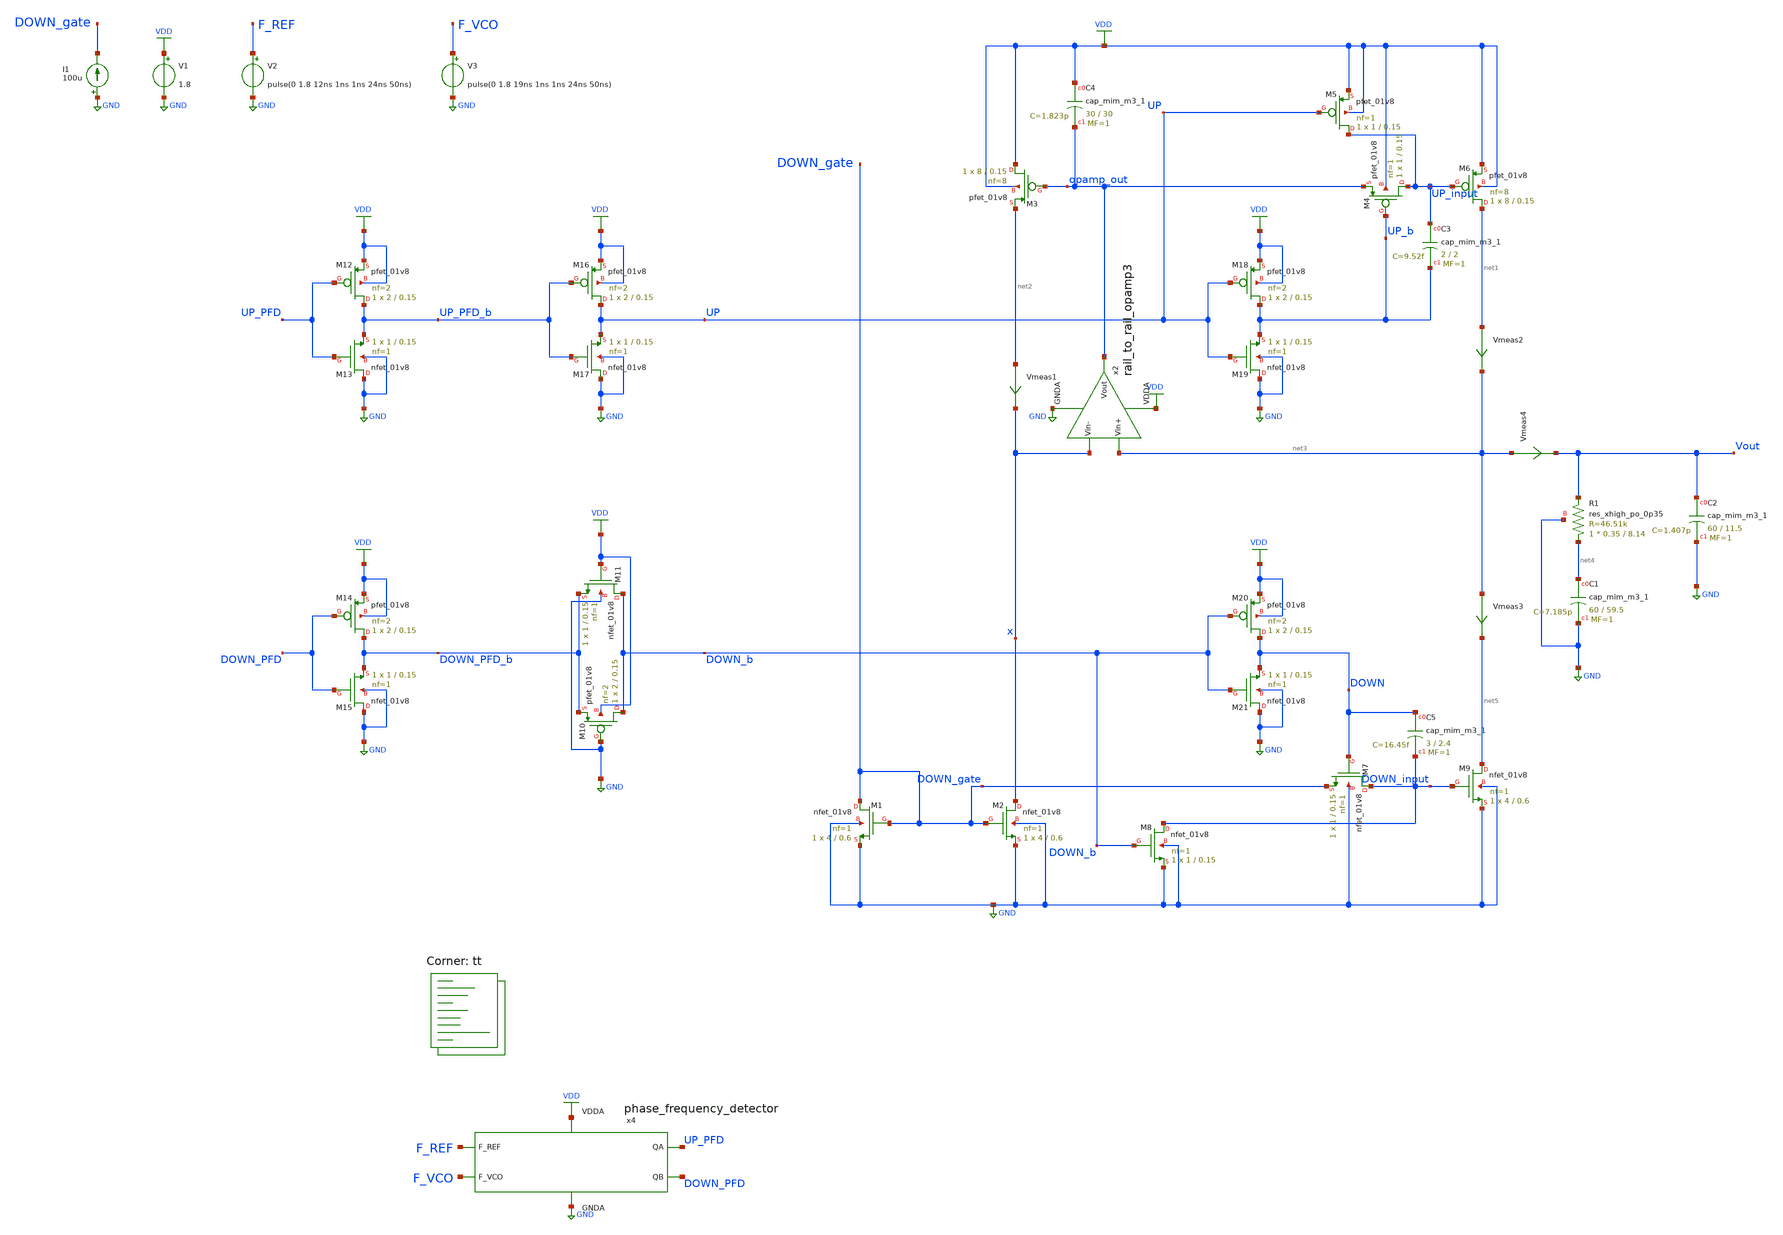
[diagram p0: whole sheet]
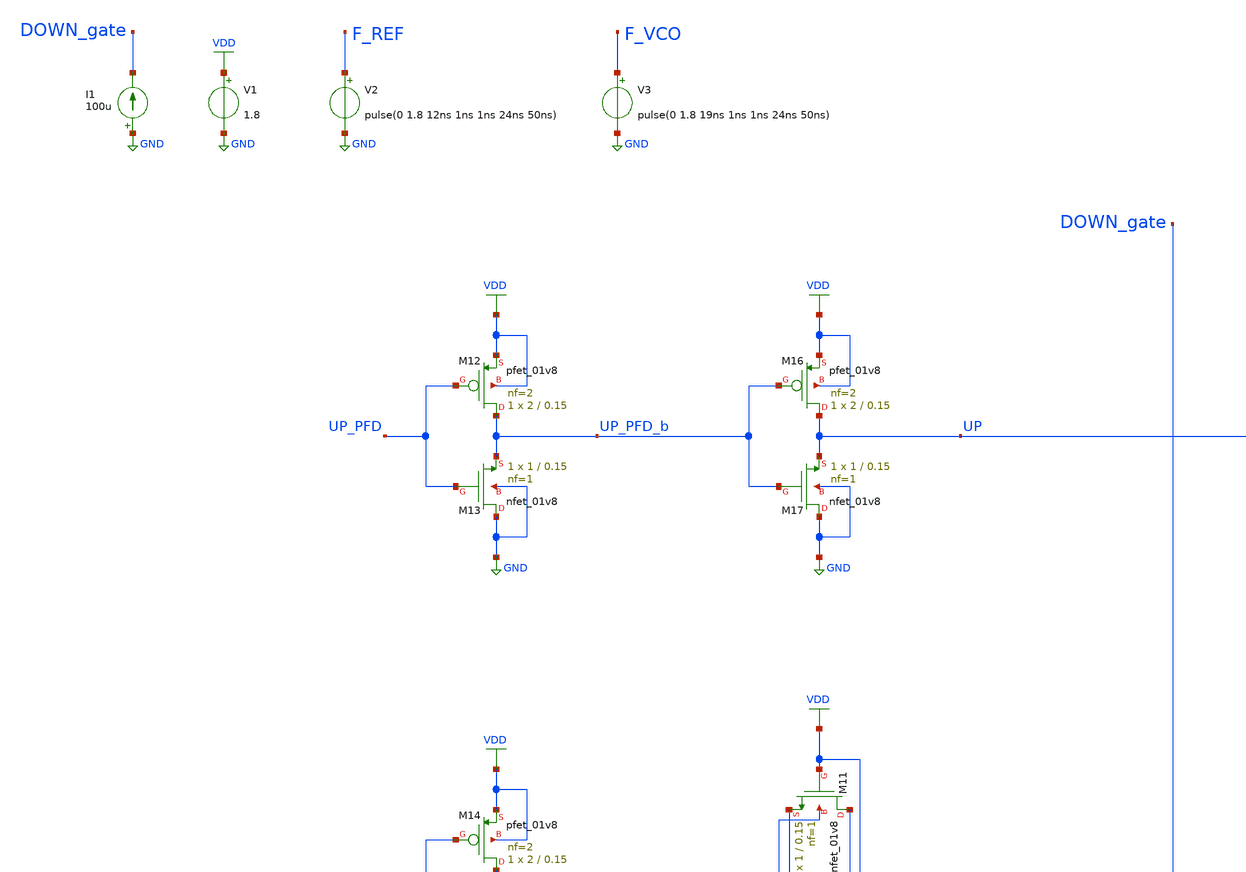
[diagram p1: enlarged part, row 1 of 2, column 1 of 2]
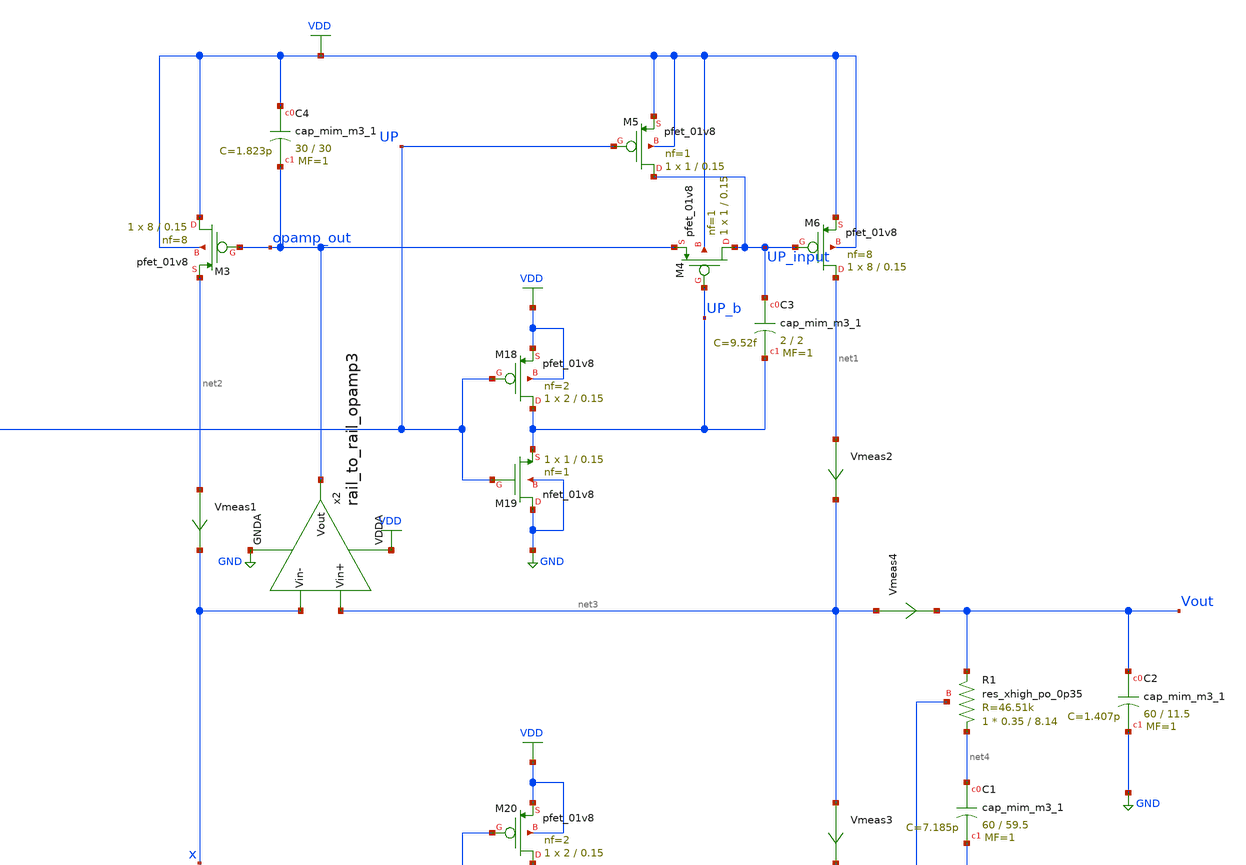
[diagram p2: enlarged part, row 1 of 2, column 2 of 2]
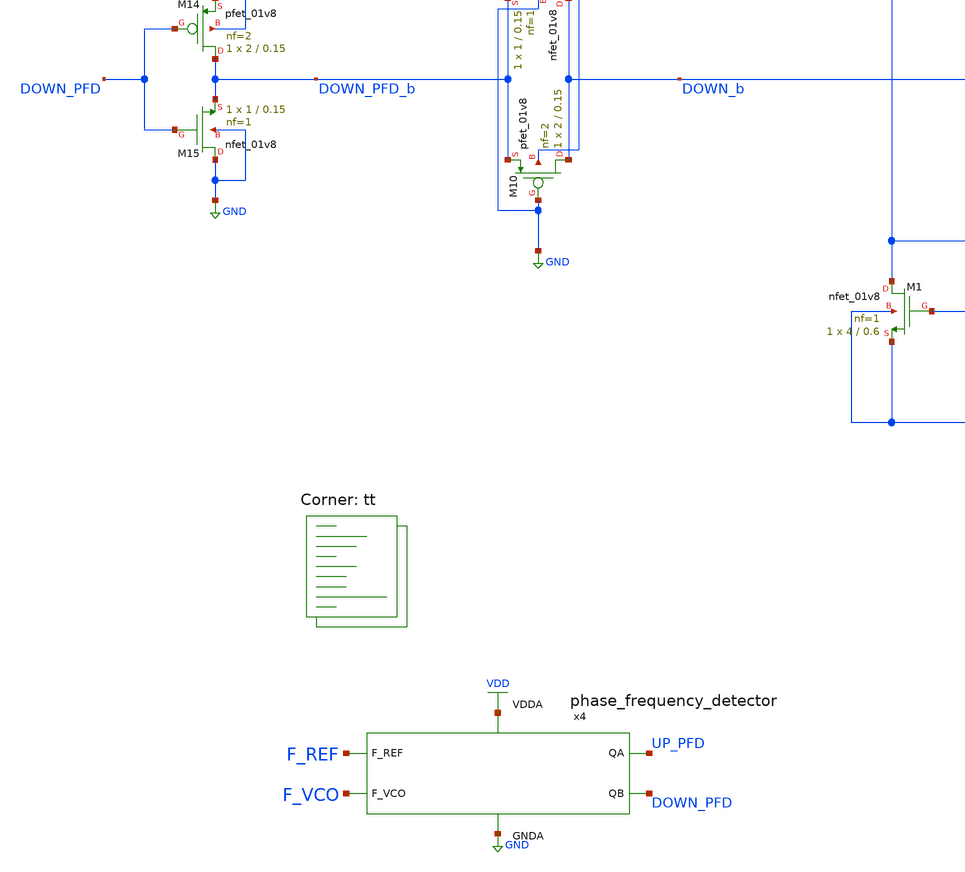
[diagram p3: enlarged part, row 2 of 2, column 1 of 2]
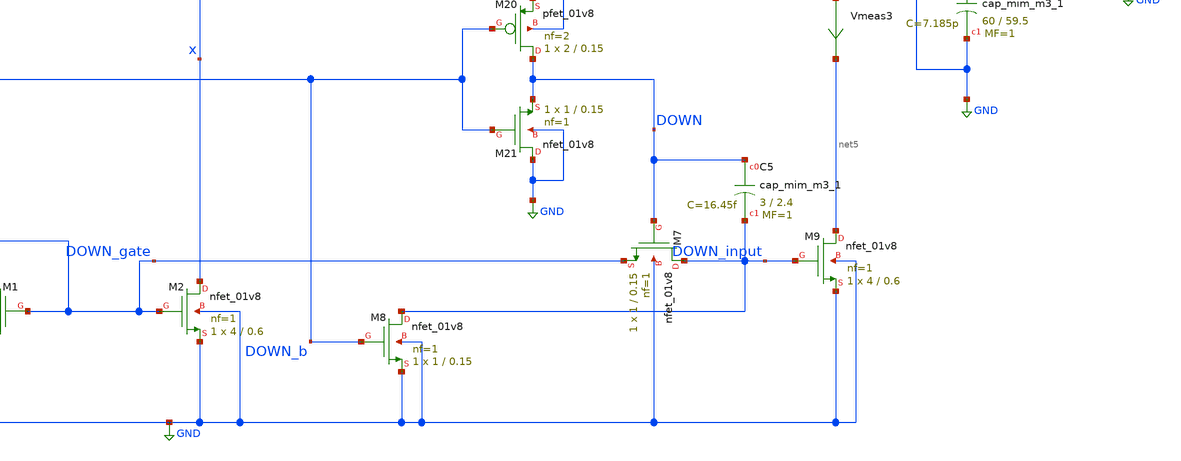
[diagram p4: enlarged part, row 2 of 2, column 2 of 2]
** sch_path: projects/pll/charge_pump/xschem_ngspice/pfd_charge_pump_7_2.sch
**.subckt pfd_charge_pump_7_2
V1 VDD GND 1.8
V2 F_REF GND pulse(0 1.8 12ns 1ns 1ns 24ns 50ns)
V3 F_VCO GND pulse(0 1.8 19ns 1ns 1ns 24ns 50ns)
x4 F_REF F_VCO VDD UP_PFD DOWN_PFD GND phase_frequency_detector
I1 GND DOWN_gate 100u
XM1 DOWN_gate DOWN_gate GND GND sky130_fd_pr__nfet_01v8 L=0.6 W=4 nf=1 ad='int((nf+1)/2) * W/nf * 0.29'
+ as='int((nf+2)/2) * W/nf * 0.29' pd='2*int((nf+1)/2) * (W/nf + 0.29)' ps='2*int((nf+2)/2) * (W/nf + 0.29)'
+ nrd='0.29 / W' nrs='0.29 / W' sa=0 sb=0 sd=0 mult=1 m=1
XM2 x DOWN_gate GND GND sky130_fd_pr__nfet_01v8 L=0.6 W=4 nf=1 ad='int((nf+1)/2) * W/nf * 0.29' as='int((nf+2)/2) * W/nf * 0.29'
+ pd='2*int((nf+1)/2) * (W/nf + 0.29)' ps='2*int((nf+2)/2) * (W/nf + 0.29)' nrd='0.29 / W' nrs='0.29 / W'
+ sa=0 sb=0 sd=0 mult=1 m=1
XM3 VDD opamp_out net2 VDD sky130_fd_pr__pfet_01v8 L=0.15 W=8 nf=8 ad='int((nf+1)/2) * W/nf * 0.29' as='int((nf+2)/2) * W/nf * 0.29'
+ pd='2*int((nf+1)/2) * (W/nf + 0.29)' ps='2*int((nf+2)/2) * (W/nf + 0.29)' nrd='0.29 / W' nrs='0.29 / W'
+ sa=0 sb=0 sd=0 mult=1 m=1
Vmeas1 net2 x 0
.save i(vmeas1)
XM4 UP_input UP_b opamp_out VDD sky130_fd_pr__pfet_01v8 L=0.15 W=1 nf=1 ad='int((nf+1)/2) * W/nf * 0.29'
+ as='int((nf+2)/2) * W/nf * 0.29' pd='2*int((nf+1)/2) * (W/nf + 0.29)' ps='2*int((nf+2)/2) * (W/nf + 0.29)'
+ nrd='0.29 / W' nrs='0.29 / W' sa=0 sb=0 sd=0 mult=1 m=1
XM5 UP_input UP VDD VDD sky130_fd_pr__pfet_01v8 L=0.15 W=1 nf=1 ad='int((nf+1)/2) * W/nf * 0.29' as='int((nf+2)/2) * W/nf * 0.29'
+ pd='2*int((nf+1)/2) * (W/nf + 0.29)' ps='2*int((nf+2)/2) * (W/nf + 0.29)' nrd='0.29 / W' nrs='0.29 / W'
+ sa=0 sb=0 sd=0 mult=1 m=1
XM6 net1 UP_input VDD VDD sky130_fd_pr__pfet_01v8 L=0.15 W=8 nf=8 ad='int((nf+1)/2) * W/nf * 0.29' as='int((nf+2)/2) * W/nf * 0.29'
+ pd='2*int((nf+1)/2) * (W/nf + 0.29)' ps='2*int((nf+2)/2) * (W/nf + 0.29)' nrd='0.29 / W' nrs='0.29 / W'
+ sa=0 sb=0 sd=0 mult=1 m=1
Vmeas2 net1 net3 0
.save i(vmeas2)
XM7 DOWN_input DOWN DOWN_gate GND sky130_fd_pr__nfet_01v8 L=0.15 W=1 nf=1 ad='int((nf+1)/2) * W/nf * 0.29'
+ as='int((nf+2)/2) * W/nf * 0.29' pd='2*int((nf+1)/2) * (W/nf + 0.29)' ps='2*int((nf+2)/2) * (W/nf + 0.29)'
+ nrd='0.29 / W' nrs='0.29 / W' sa=0 sb=0 sd=0 mult=1 m=1
XM8 DOWN_input DOWN_b GND GND sky130_fd_pr__nfet_01v8 L=0.15 W=1 nf=1 ad='int((nf+1)/2) * W/nf * 0.29'
+ as='int((nf+2)/2) * W/nf * 0.29' pd='2*int((nf+1)/2) * (W/nf + 0.29)' ps='2*int((nf+2)/2) * (W/nf + 0.29)'
+ nrd='0.29 / W' nrs='0.29 / W' sa=0 sb=0 sd=0 mult=1 m=1
Vmeas3 net3 net5 0
.save i(vmeas3)
XM9 net5 DOWN_input GND GND sky130_fd_pr__nfet_01v8 L=0.6 W=4 nf=1 ad='int((nf+1)/2) * W/nf * 0.29' as='int((nf+2)/2) * W/nf * 0.29'
+ pd='2*int((nf+1)/2) * (W/nf + 0.29)' ps='2*int((nf+2)/2) * (W/nf + 0.29)' nrd='0.29 / W' nrs='0.29 / W'
+ sa=0 sb=0 sd=0 mult=1 m=1
XC2 Vout GND sky130_fd_pr__cap_mim_m3_1 W=60 L=11.5 MF=1 m=1
XC1 net4 GND sky130_fd_pr__cap_mim_m3_1 W=60 L=59.5 MF=1 m=1
Vmeas4 net3 Vout 0
.save i(vmeas4)
x2 VDD net3 x opamp_out GND rail_to_rail_opamp3
XC4 VDD opamp_out sky130_fd_pr__cap_mim_m3_1 W=30 L=30 MF=1 m=1
XC3 UP_input UP_b sky130_fd_pr__cap_mim_m3_1 W=2 L=2 MF=1 m=1
XC5 DOWN DOWN_input sky130_fd_pr__cap_mim_m3_1 W=3 L=2.4 MF=1 m=1
XM10 DOWN_b GND DOWN_PFD_b VDD sky130_fd_pr__pfet_01v8 L=0.15 W=2 nf=2 ad='int((nf+1)/2) * W/nf * 0.29'
+ as='int((nf+2)/2) * W/nf * 0.29' pd='2*int((nf+1)/2) * (W/nf + 0.29)' ps='2*int((nf+2)/2) * (W/nf + 0.29)'
+ nrd='0.29 / W' nrs='0.29 / W' sa=0 sb=0 sd=0 mult=1 m=1
XM11 DOWN_b VDD DOWN_PFD_b GND sky130_fd_pr__nfet_01v8 L=0.15 W=1 nf=1 ad='int((nf+1)/2) * W/nf * 0.29'
+ as='int((nf+2)/2) * W/nf * 0.29' pd='2*int((nf+1)/2) * (W/nf + 0.29)' ps='2*int((nf+2)/2) * (W/nf + 0.29)'
+ nrd='0.29 / W' nrs='0.29 / W' sa=0 sb=0 sd=0 mult=1 m=1
XM12 UP_PFD_b UP_PFD VDD VDD sky130_fd_pr__pfet_01v8 L=0.15 W=2 nf=2 ad='int((nf+1)/2) * W/nf * 0.29'
+ as='int((nf+2)/2) * W/nf * 0.29' pd='2*int((nf+1)/2) * (W/nf + 0.29)' ps='2*int((nf+2)/2) * (W/nf + 0.29)'
+ nrd='0.29 / W' nrs='0.29 / W' sa=0 sb=0 sd=0 mult=1 m=1
XM13 GND UP_PFD UP_PFD_b GND sky130_fd_pr__nfet_01v8 L=0.15 W=1 nf=1 ad='int((nf+1)/2) * W/nf * 0.29'
+ as='int((nf+2)/2) * W/nf * 0.29' pd='2*int((nf+1)/2) * (W/nf + 0.29)' ps='2*int((nf+2)/2) * (W/nf + 0.29)'
+ nrd='0.29 / W' nrs='0.29 / W' sa=0 sb=0 sd=0 mult=1 m=1
XM14 DOWN_PFD_b DOWN_PFD VDD VDD sky130_fd_pr__pfet_01v8 L=0.15 W=2 nf=2 ad='int((nf+1)/2) * W/nf * 0.29'
+ as='int((nf+2)/2) * W/nf * 0.29' pd='2*int((nf+1)/2) * (W/nf + 0.29)' ps='2*int((nf+2)/2) * (W/nf + 0.29)'
+ nrd='0.29 / W' nrs='0.29 / W' sa=0 sb=0 sd=0 mult=1 m=1
XM15 GND DOWN_PFD DOWN_PFD_b GND sky130_fd_pr__nfet_01v8 L=0.15 W=1 nf=1 ad='int((nf+1)/2) * W/nf * 0.29'
+ as='int((nf+2)/2) * W/nf * 0.29' pd='2*int((nf+1)/2) * (W/nf + 0.29)' ps='2*int((nf+2)/2) * (W/nf + 0.29)'
+ nrd='0.29 / W' nrs='0.29 / W' sa=0 sb=0 sd=0 mult=1 m=1
XM16 UP UP_PFD_b VDD VDD sky130_fd_pr__pfet_01v8 L=0.15 W=2 nf=2 ad='int((nf+1)/2) * W/nf * 0.29' as='int((nf+2)/2) * W/nf * 0.29'
+ pd='2*int((nf+1)/2) * (W/nf + 0.29)' ps='2*int((nf+2)/2) * (W/nf + 0.29)' nrd='0.29 / W' nrs='0.29 / W'
+ sa=0 sb=0 sd=0 mult=1 m=1
XM17 GND UP_PFD_b UP GND sky130_fd_pr__nfet_01v8 L=0.15 W=1 nf=1 ad='int((nf+1)/2) * W/nf * 0.29' as='int((nf+2)/2) * W/nf * 0.29'
+ pd='2*int((nf+1)/2) * (W/nf + 0.29)' ps='2*int((nf+2)/2) * (W/nf + 0.29)' nrd='0.29 / W' nrs='0.29 / W'
+ sa=0 sb=0 sd=0 mult=1 m=1
XM18 UP_b UP VDD VDD sky130_fd_pr__pfet_01v8 L=0.15 W=2 nf=2 ad='int((nf+1)/2) * W/nf * 0.29' as='int((nf+2)/2) * W/nf * 0.29'
+ pd='2*int((nf+1)/2) * (W/nf + 0.29)' ps='2*int((nf+2)/2) * (W/nf + 0.29)' nrd='0.29 / W' nrs='0.29 / W'
+ sa=0 sb=0 sd=0 mult=1 m=1
XM19 GND UP UP_b GND sky130_fd_pr__nfet_01v8 L=0.15 W=1 nf=1 ad='int((nf+1)/2) * W/nf * 0.29' as='int((nf+2)/2) * W/nf * 0.29'
+ pd='2*int((nf+1)/2) * (W/nf + 0.29)' ps='2*int((nf+2)/2) * (W/nf + 0.29)' nrd='0.29 / W' nrs='0.29 / W'
+ sa=0 sb=0 sd=0 mult=1 m=1
XM20 DOWN DOWN_b VDD VDD sky130_fd_pr__pfet_01v8 L=0.15 W=2 nf=2 ad='int((nf+1)/2) * W/nf * 0.29' as='int((nf+2)/2) * W/nf * 0.29'
+ pd='2*int((nf+1)/2) * (W/nf + 0.29)' ps='2*int((nf+2)/2) * (W/nf + 0.29)' nrd='0.29 / W' nrs='0.29 / W'
+ sa=0 sb=0 sd=0 mult=1 m=1
XM21 GND DOWN_b DOWN GND sky130_fd_pr__nfet_01v8 L=0.15 W=1 nf=1 ad='int((nf+1)/2) * W/nf * 0.29' as='int((nf+2)/2) * W/nf * 0.29'
+ pd='2*int((nf+1)/2) * (W/nf + 0.29)' ps='2*int((nf+2)/2) * (W/nf + 0.29)' nrd='0.29 / W' nrs='0.29 / W'
+ sa=0 sb=0 sd=0 mult=1 m=1
XR1 net4 Vout GND sky130_fd_pr__res_xhigh_po_0p35 L=8.14 mult=1 m=1
**** begin user architecture code
.lib $::SKYWATER_MODELS/sky130.lib.spice tt



.include /foss/pdks/sky130A/libs.ref/sky130_fd_sc_hd/spice/sky130_fd_sc_hd.spice

.option method=gear
.option wnflag=1

.ic v(vout) = 0.9
* .ic v(vout) = 1.8

.control
  save v(up_pfd) v(down_pfd) v(up_pfd_b) v(down_pfd_b) v(up) v(up_b) v(down) v(down_b) v(x) v(vout)
+ v(up_input) v(down_input)
  * save all

  tran 50ps 0.5us
  remzerovec
  write pfd_charge_pump_7_2.raw
  set appendwrite

.endc



**** end user architecture code
**.ends

* expanding   symbol:
*+  /foss/designs/my_design/projects/pll/pfd/xschem_ngspice/phase_frequency_detector.sym # of pins=6
** sym_path: projects/pll/pfd/xschem_ngspice/phase_frequency_detector.sym
** sch_path: projects/pll/pfd/xschem_ngspice/phase_frequency_detector.sch
.subckt phase_frequency_detector F_REF F_VCO VDDA QA QB GNDA
*.ipin F_REF
*.opin QA
*.ipin F_VCO
*.opin QB
*.ipin VDDA
*.ipin GNDA
x1 F_REF QA GNDA GNDA VDDA VDDA QA_b sky130_fd_sc_hd__nor2_1
x2 QA_b E GNDA GNDA VDDA VDDA QA sky130_fd_sc_hd__nor2_1
x3 QA_b E_b GNDA GNDA VDDA VDDA E sky130_fd_sc_hd__nor2_1
x4 E Reset GNDA GNDA VDDA VDDA E_b sky130_fd_sc_hd__nor2_1
x5 F_VCO QB GNDA GNDA VDDA VDDA QB_b sky130_fd_sc_hd__nor2_1
x6 QB_b F GNDA GNDA VDDA VDDA QB sky130_fd_sc_hd__nor2_1
x7 QB_b F_b GNDA GNDA VDDA VDDA F sky130_fd_sc_hd__nor2_1
x8 F Reset GNDA GNDA VDDA VDDA F_b sky130_fd_sc_hd__nor2_1
x9 QA QB GNDA GNDA VDDA VDDA before_Reset sky130_fd_sc_hd__nand2_1
x10 before_Reset GNDA GNDA VDDA VDDA net1 sky130_fd_sc_hd__inv_1
x11 net1 GNDA GNDA VDDA VDDA net2 sky130_fd_sc_hd__inv_1
x12 net2 GNDA GNDA VDDA VDDA net3 sky130_fd_sc_hd__inv_1
x13 net3 GNDA GNDA VDDA VDDA net4 sky130_fd_sc_hd__inv_1
x14 net4 GNDA GNDA VDDA VDDA Reset sky130_fd_sc_hd__inv_1
.ends


* expanding   symbol:
*+  /foss/designs/my_design/projects/pll/charge_pump/xschem_ngspice/rail_to_rail_opamp3.sym # of pins=5
** sym_path: projects/pll/charge_pump/xschem_ngspice/rail_to_rail_opamp3.sym
** sch_path: projects/pll/charge_pump/xschem_ngspice/rail_to_rail_opamp3.sch
.subckt rail_to_rail_opamp3 VDDA Vin+ Vin- Vout GNDA
*.opin Vout
*.ipin Vin+
*.ipin Vin-
*.ipin VDDA
*.ipin GNDA
XM2 n_left Vin+ v_common_n GNDA sky130_fd_pr__nfet_01v8 L=0.15 W=1 nf=1 ad='int((nf+1)/2) * W/nf * 0.29'
+ as='int((nf+2)/2) * W/nf * 0.29' pd='2*int((nf+1)/2) * (W/nf + 0.29)' ps='2*int((nf+2)/2) * (W/nf + 0.29)'
+ nrd='0.29 / W' nrs='0.29 / W' sa=0 sb=0 sd=0 mult=1 m=1
XM3 n_right Vin- v_common_n GNDA sky130_fd_pr__nfet_01v8 L=0.15 W=1 nf=1 ad='int((nf+1)/2) * W/nf * 0.29'
+ as='int((nf+2)/2) * W/nf * 0.29' pd='2*int((nf+1)/2) * (W/nf + 0.29)' ps='2*int((nf+2)/2) * (W/nf + 0.29)'
+ nrd='0.29 / W' nrs='0.29 / W' sa=0 sb=0 sd=0 mult=1 m=1
XM5 n_left n_left VDDA VDDA sky130_fd_pr__pfet_01v8 L=0.15 W=2 nf=2 ad='int((nf+1)/2) * W/nf * 0.29'
+ as='int((nf+2)/2) * W/nf * 0.29' pd='2*int((nf+1)/2) * (W/nf + 0.29)' ps='2*int((nf+2)/2) * (W/nf + 0.29)'
+ nrd='0.29 / W' nrs='0.29 / W' sa=0 sb=0 sd=0 mult=1 m=1
XM4 n_right n_left VDDA VDDA sky130_fd_pr__pfet_01v8 L=0.15 W=2 nf=2 ad='int((nf+1)/2) * W/nf * 0.29'
+ as='int((nf+2)/2) * W/nf * 0.29' pd='2*int((nf+1)/2) * (W/nf + 0.29)' ps='2*int((nf+2)/2) * (W/nf + 0.29)'
+ nrd='0.29 / W' nrs='0.29 / W' sa=0 sb=0 sd=0 mult=1 m=1
XM6 v_common_p p_bias VDDA VDDA sky130_fd_pr__pfet_01v8 L=0.15 W=3 nf=3 ad='int((nf+1)/2) * W/nf * 0.29'
+ as='int((nf+2)/2) * W/nf * 0.29' pd='2*int((nf+1)/2) * (W/nf + 0.29)' ps='2*int((nf+2)/2) * (W/nf + 0.29)'
+ nrd='0.29 / W' nrs='0.29 / W' sa=0 sb=0 sd=0 mult=1 m=1
XM7 p_left Vin+ v_common_p VDDA sky130_fd_pr__pfet_01v8 L=0.15 W=2 nf=2 ad='int((nf+1)/2) * W/nf * 0.29'
+ as='int((nf+2)/2) * W/nf * 0.29' pd='2*int((nf+1)/2) * (W/nf + 0.29)' ps='2*int((nf+2)/2) * (W/nf + 0.29)'
+ nrd='0.29 / W' nrs='0.29 / W' sa=0 sb=0 sd=0 mult=1 m=1
XM8 p_right Vin- v_common_p VDDA sky130_fd_pr__pfet_01v8 L=0.15 W=2 nf=2 ad='int((nf+1)/2) * W/nf * 0.29'
+ as='int((nf+2)/2) * W/nf * 0.29' pd='2*int((nf+1)/2) * (W/nf + 0.29)' ps='2*int((nf+2)/2) * (W/nf + 0.29)'
+ nrd='0.29 / W' nrs='0.29 / W' sa=0 sb=0 sd=0 mult=1 m=1
XM9 p_left p_left GNDA GNDA sky130_fd_pr__nfet_01v8 L=0.15 W=1 nf=1 ad='int((nf+1)/2) * W/nf * 0.29'
+ as='int((nf+2)/2) * W/nf * 0.29' pd='2*int((nf+1)/2) * (W/nf + 0.29)' ps='2*int((nf+2)/2) * (W/nf + 0.29)'
+ nrd='0.29 / W' nrs='0.29 / W' sa=0 sb=0 sd=0 mult=1 m=1
XM10 p_right p_left GNDA GNDA sky130_fd_pr__nfet_01v8 L=0.15 W=1 nf=1 ad='int((nf+1)/2) * W/nf * 0.29'
+ as='int((nf+2)/2) * W/nf * 0.29' pd='2*int((nf+1)/2) * (W/nf + 0.29)' ps='2*int((nf+2)/2) * (W/nf + 0.29)'
+ nrd='0.29 / W' nrs='0.29 / W' sa=0 sb=0 sd=0 mult=1 m=1
XM1 v_common_n n_bias GNDA GNDA sky130_fd_pr__nfet_01v8 L=0.15 W=1 nf=1 ad='int((nf+1)/2) * W/nf * 0.29'
+ as='int((nf+2)/2) * W/nf * 0.29' pd='2*int((nf+1)/2) * (W/nf + 0.29)' ps='2*int((nf+2)/2) * (W/nf + 0.29)'
+ nrd='0.29 / W' nrs='0.29 / W' sa=0 sb=0 sd=0 mult=1 m=1
XM11 Vout n_right VDDA VDDA sky130_fd_pr__pfet_01v8 L=0.15 W=16 nf=2 ad='int((nf+1)/2) * W/nf * 0.29'
+ as='int((nf+2)/2) * W/nf * 0.29' pd='2*int((nf+1)/2) * (W/nf + 0.29)' ps='2*int((nf+2)/2) * (W/nf + 0.29)'
+ nrd='0.29 / W' nrs='0.29 / W' sa=0 sb=0 sd=0 mult=1 m=1
XM12 Vout p_right GNDA GNDA sky130_fd_pr__nfet_01v8 L=0.15 W=8 nf=1 ad='int((nf+1)/2) * W/nf * 0.29'
+ as='int((nf+2)/2) * W/nf * 0.29' pd='2*int((nf+1)/2) * (W/nf + 0.29)' ps='2*int((nf+2)/2) * (W/nf + 0.29)'
+ nrd='0.29 / W' nrs='0.29 / W' sa=0 sb=0 sd=0 mult=1 m=1
XM13 n_bias n_bias GNDA GNDA sky130_fd_pr__nfet_01v8 L=0.15 W=1 nf=1 ad='int((nf+1)/2) * W/nf * 0.29'
+ as='int((nf+2)/2) * W/nf * 0.29' pd='2*int((nf+1)/2) * (W/nf + 0.29)' ps='2*int((nf+2)/2) * (W/nf + 0.29)'
+ nrd='0.29 / W' nrs='0.29 / W' sa=0 sb=0 sd=0 mult=1 m=1
XM15 p_bias p_bias VDDA VDDA sky130_fd_pr__pfet_01v8 L=0.15 W=2 nf=2 ad='int((nf+1)/2) * W/nf * 0.29'
+ as='int((nf+2)/2) * W/nf * 0.29' pd='2*int((nf+1)/2) * (W/nf + 0.29)' ps='2*int((nf+2)/2) * (W/nf + 0.29)'
+ nrd='0.29 / W' nrs='0.29 / W' sa=0 sb=0 sd=0 mult=1 m=1
Vmeas net1 n_bias 0
.save i(vmeas)
XM14 net1 net1 p_bias p_bias sky130_fd_pr__pfet_01v8 L=0.15 W=2 nf=2 ad='int((nf+1)/2) * W/nf * 0.29'
+ as='int((nf+2)/2) * W/nf * 0.29' pd='2*int((nf+1)/2) * (W/nf + 0.29)' ps='2*int((nf+2)/2) * (W/nf + 0.29)'
+ nrd='0.29 / W' nrs='0.29 / W' sa=0 sb=0 sd=0 mult=1 m=1
.ends

.GLOBAL GND
.GLOBAL VDD
.end
